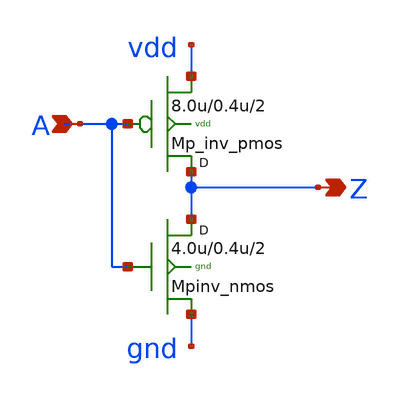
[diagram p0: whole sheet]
** sch_path: sram_2_16_scn4m/pinv_9.sch
**.subckt pinv_9 A Z
*.ipin A
*.opin Z
Mpinv_nmos Z A gnd gnd n w=4.0u l=0.4u m=2
Mp_inv_pmos Z A vdd vdd p w=8.0u l=0.4u m=2
**.ends
.end
